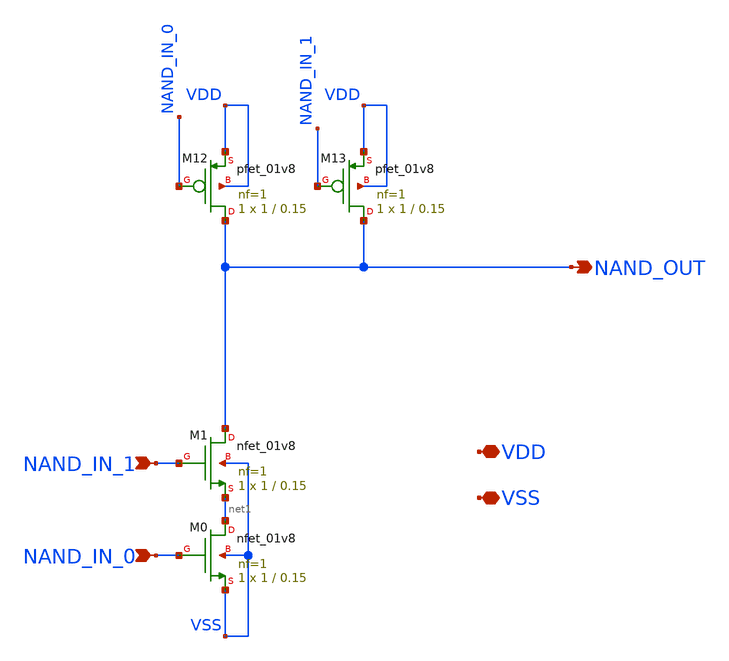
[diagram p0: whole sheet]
** sch_path: xschem/NAND2.sch
**.subckt NAND2 NAND_IN_0 NAND_OUT VDD VSS NAND_IN_1
*.ipin NAND_IN_0
*.opin NAND_OUT
*.iopin VDD
*.iopin VSS
*.ipin NAND_IN_1
XM0 net1 NAND_IN_0 VSS VSS sky130_fd_pr__nfet_01v8 L=0.15 W=1 nf=1 ad='int((nf+1)/2) * W/nf * 0.29' as='int((nf+2)/2) * W/nf * 0.29'
+ pd='2*int((nf+1)/2) * (W/nf + 0.29)' ps='2*int((nf+2)/2) * (W/nf + 0.29)' nrd='0.29 / W' nrs='0.29 / W'
+ sa=0 sb=0 sd=0 mult=1 m=1
XM1 NAND_OUT NAND_IN_1 net1 VSS sky130_fd_pr__nfet_01v8 L=0.15 W=1 nf=1 ad='int((nf+1)/2) * W/nf * 0.29'
+ as='int((nf+2)/2) * W/nf * 0.29' pd='2*int((nf+1)/2) * (W/nf + 0.29)' ps='2*int((nf+2)/2) * (W/nf + 0.29)'
+ nrd='0.29 / W' nrs='0.29 / W' sa=0 sb=0 sd=0 mult=1 m=1
XM12 NAND_OUT NAND_IN_0 VDD VDD sky130_fd_pr__pfet_01v8 L=0.15 W=1 nf=1 ad='int((nf+1)/2) * W/nf * 0.29'
+ as='int((nf+2)/2) * W/nf * 0.29' pd='2*int((nf+1)/2) * (W/nf + 0.29)' ps='2*int((nf+2)/2) * (W/nf + 0.29)'
+ nrd='0.29 / W' nrs='0.29 / W' sa=0 sb=0 sd=0 mult=1 m=1
XM13 NAND_OUT NAND_IN_1 VDD VDD sky130_fd_pr__pfet_01v8 L=0.15 W=1 nf=1 ad='int((nf+1)/2) * W/nf * 0.29'
+ as='int((nf+2)/2) * W/nf * 0.29' pd='2*int((nf+1)/2) * (W/nf + 0.29)' ps='2*int((nf+2)/2) * (W/nf + 0.29)'
+ nrd='0.29 / W' nrs='0.29 / W' sa=0 sb=0 sd=0 mult=1 m=1
**.ends
.end
